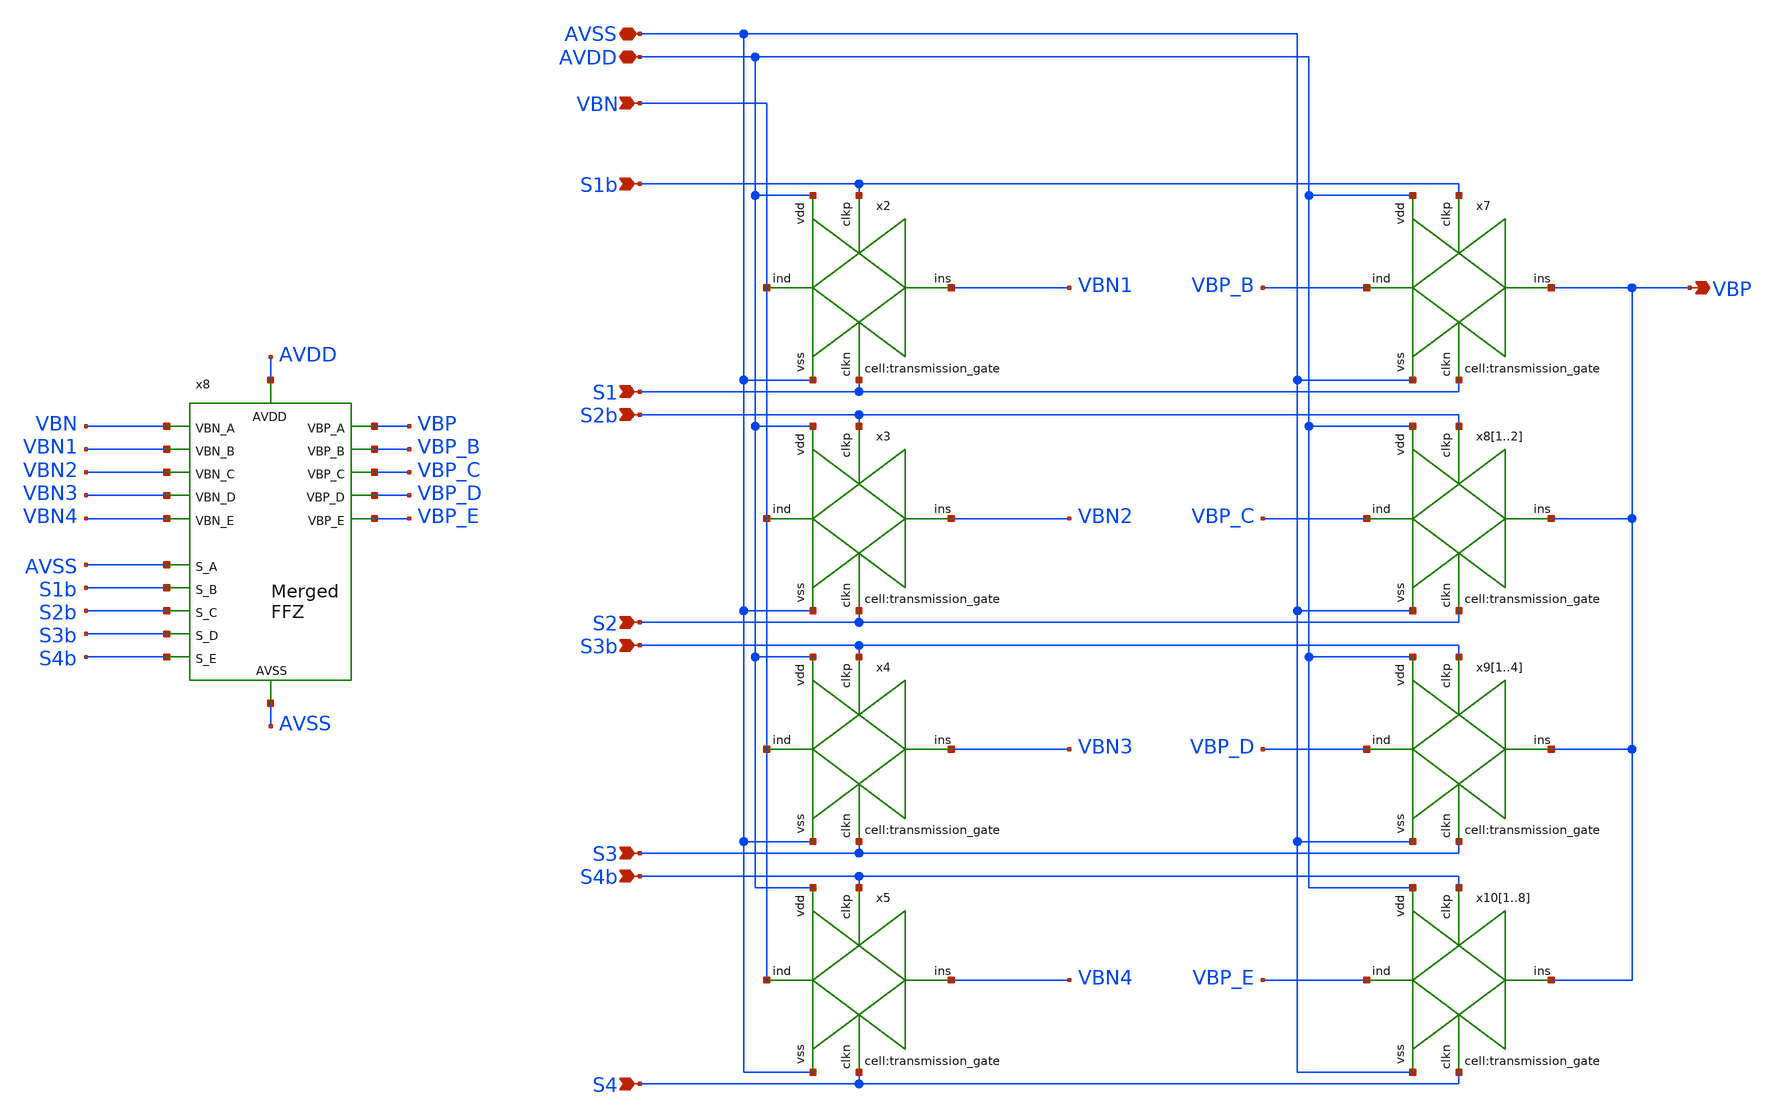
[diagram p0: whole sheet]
** sch_path: designs/libs/core_analog/programmable_ffz/programmable_ffz_v2.sch
**.subckt programmable_ffz_v2 VBN S1b S1 S2b S2 S3b S3 S4b S4 AVSS AVDD VBP
*.ipin VBN
*.ipin S1b
*.ipin S1
*.ipin S2b
*.ipin S2
*.ipin S3b
*.ipin S3
*.ipin S4b
*.ipin S4
*.iopin AVSS
*.iopin AVDD
*.opin VBP
x2 VBN AVSS S1 VBN1 S1b AVDD transmission_gate
x3 VBN AVSS S2 VBN2 S2b AVDD transmission_gate
x4 VBN AVSS S3 VBN3 S3b AVDD transmission_gate
x5 VBN AVSS S4 VBN4 S4b AVDD transmission_gate
x7 VBP_B AVSS S1 VBP S1b AVDD transmission_gate
x81 VBP_C AVSS S2 VBP S2b AVDD transmission_gate
x82 VBP_C AVSS S2 VBP S2b AVDD transmission_gate
x91 VBP_D AVSS S3 VBP S3b AVDD transmission_gate
x92 VBP_D AVSS S3 VBP S3b AVDD transmission_gate
x93 VBP_D AVSS S3 VBP S3b AVDD transmission_gate
x94 VBP_D AVSS S3 VBP S3b AVDD transmission_gate
x101 VBP_E AVSS S4 VBP S4b AVDD transmission_gate
x102 VBP_E AVSS S4 VBP S4b AVDD transmission_gate
x103 VBP_E AVSS S4 VBP S4b AVDD transmission_gate
x104 VBP_E AVSS S4 VBP S4b AVDD transmission_gate
x105 VBP_E AVSS S4 VBP S4b AVDD transmission_gate
x106 VBP_E AVSS S4 VBP S4b AVDD transmission_gate
x107 VBP_E AVSS S4 VBP S4b AVDD transmission_gate
x108 VBP_E AVSS S4 VBP S4b AVDD transmission_gate
x8 VBP_E VBP VBP_C VBN4 VBN VBN2 S4b AVSS S2b AVDD AVSS VBP_B VBP_D VBN1 VBN3 S3b S1b
+ feed_forward_zero_v2_merged
**.ends

* expanding   symbol:  libs/core_analog/transmission_gate/transmission_gate.sym # of pins=6
** sym_path: designs/libs/core_analog/transmission_gate/transmission_gate.sym
** sch_path: designs/libs/core_analog/transmission_gate/transmission_gate.sch
.subckt transmission_gate ind vss clkn ins clkp vdd
*.iopin ind
*.iopin ins
*.iopin clkn
*.iopin clkp
*.iopin vdd
*.iopin vss
XM1 ind clkp ins vdd pfet_03v3 L=0.5u W=3.0u nf=1 ad='int((nf+1)/2) * W/nf * 0.18u' as='int((nf+2)/2) * W/nf * 0.18u'
+ pd='2*int((nf+1)/2) * (W/nf + 0.18u)' ps='2*int((nf+2)/2) * (W/nf + 0.18u)' nrd='0.18u / W' nrs='0.18u / W'
+ sa=0 sb=0 sd=0 m=1
XM2 ind clkn ins vss nfet_03v3 L=0.5u W=1.0u nf=1 ad='int((nf+1)/2) * W/nf * 0.18u' as='int((nf+2)/2) * W/nf * 0.18u'
+ pd='2*int((nf+1)/2) * (W/nf + 0.18u)' ps='2*int((nf+2)/2) * (W/nf + 0.18u)' nrd='0.18u / W' nrs='0.18u / W'
+ sa=0 sb=0 sd=0 m=1
.ends


* expanding   symbol:  libs/core_analog/feed_forward_zero/feed_forward_zero_v2_merged.sym # of
*+ pins=17
** sym_path: designs/libs/core_analog/feed_forward_zero/feed_forward_zero_v2_merged.sym
** sch_path: designs/libs/core_analog/feed_forward_zero/feed_forward_zero_v2_merged.sch
.subckt feed_forward_zero_v2_merged VBP_E VBP_A VBP_C VBN_E VBN_A VBN_C S_E S_A S_C AVDD AVSS VBP_B
+ VBP_D VBN_B VBN_D S_D S_B
*.opin VBP_E
*.iopin AVDD
*.ipin VBN_A
*.opin VBP_A
*.ipin VBN_B
*.ipin S_B
*.opin VBP_B
*.ipin VBN_C
*.ipin S_C
*.opin VBP_C
*.ipin VBN_D
*.ipin S_D
*.opin VBP_D
*.ipin VBN_E
*.ipin S_E
*.ipin S_A
*.iopin AVSS
XM1 VBP_A VBP_A AVDD AVDD pfet_03v3 L=1.5u W=1.1u nf=1 ad='int((nf+1)/2) * W/nf * 0.18u' as='int((nf+2)/2) * W/nf * 0.18u'
+ pd='2*int((nf+1)/2) * (W/nf + 0.18u)' ps='2*int((nf+2)/2) * (W/nf + 0.18u)' nrd='0.18u / W' nrs='0.18u / W'
+ sa=0 sb=0 sd=0 m=1
XM3 VBP_A AVDD net1 AVSS nfet_03v3 L=0.5u W=2.08u nf=1 ad='int((nf+1)/2) * W/nf * 0.18u' as='int((nf+2)/2) * W/nf * 0.18u'
+ pd='2*int((nf+1)/2) * (W/nf + 0.18u)' ps='2*int((nf+2)/2) * (W/nf + 0.18u)' nrd='0.18u / W' nrs='0.18u / W'
+ sa=0 sb=0 sd=0 m=1
XM4 net1 VBN_A AVSS AVSS nfet_03v3 L=0.5u W=2.82u nf=1 ad='int((nf+1)/2) * W/nf * 0.18u' as='int((nf+2)/2) * W/nf * 0.18u'
+ pd='2*int((nf+1)/2) * (W/nf + 0.18u)' ps='2*int((nf+2)/2) * (W/nf + 0.18u)' nrd='0.18u / W' nrs='0.18u / W'
+ sa=0 sb=0 sd=0 m=4
XM7 VBN_A S_A AVSS AVSS nfet_03v3 L=0.5u W=1u nf=1 ad='int((nf+1)/2) * W/nf * 0.18u' as='int((nf+2)/2) * W/nf * 0.18u'
+ pd='2*int((nf+1)/2) * (W/nf + 0.18u)' ps='2*int((nf+2)/2) * (W/nf + 0.18u)' nrd='0.18u / W' nrs='0.18u / W'
+ sa=0 sb=0 sd=0 m=1
XM2 VBP_A VBP_A AVDD AVDD pfet_03v3 L=1.5u W=1.1u nf=1 ad='int((nf+1)/2) * W/nf * 0.18u' as='int((nf+2)/2) * W/nf * 0.18u'
+ pd='2*int((nf+1)/2) * (W/nf + 0.18u)' ps='2*int((nf+2)/2) * (W/nf + 0.18u)' nrd='0.18u / W' nrs='0.18u / W'
+ sa=0 sb=0 sd=0 m=1
XM5 VBP_B VBP_B AVDD AVDD pfet_03v3 L=1.5u W=1.1u nf=1 ad='int((nf+1)/2) * W/nf * 0.18u' as='int((nf+2)/2) * W/nf * 0.18u'
+ pd='2*int((nf+1)/2) * (W/nf + 0.18u)' ps='2*int((nf+2)/2) * (W/nf + 0.18u)' nrd='0.18u / W' nrs='0.18u / W'
+ sa=0 sb=0 sd=0 m=1
XM6 VBP_B AVDD net2 AVSS nfet_03v3 L=0.5u W=2.08u nf=1 ad='int((nf+1)/2) * W/nf * 0.18u' as='int((nf+2)/2) * W/nf * 0.18u'
+ pd='2*int((nf+1)/2) * (W/nf + 0.18u)' ps='2*int((nf+2)/2) * (W/nf + 0.18u)' nrd='0.18u / W' nrs='0.18u / W'
+ sa=0 sb=0 sd=0 m=1
XM8 net2 VBN_B AVSS AVSS nfet_03v3 L=0.5u W=2.82u nf=1 ad='int((nf+1)/2) * W/nf * 0.18u' as='int((nf+2)/2) * W/nf * 0.18u'
+ pd='2*int((nf+1)/2) * (W/nf + 0.18u)' ps='2*int((nf+2)/2) * (W/nf + 0.18u)' nrd='0.18u / W' nrs='0.18u / W'
+ sa=0 sb=0 sd=0 m=4
XM9 VBN_B S_B AVSS AVSS nfet_03v3 L=0.5u W=1u nf=1 ad='int((nf+1)/2) * W/nf * 0.18u' as='int((nf+2)/2) * W/nf * 0.18u'
+ pd='2*int((nf+1)/2) * (W/nf + 0.18u)' ps='2*int((nf+2)/2) * (W/nf + 0.18u)' nrd='0.18u / W' nrs='0.18u / W'
+ sa=0 sb=0 sd=0 m=1
XM10 VBP_B VBP_B AVDD AVDD pfet_03v3 L=1.5u W=1.1u nf=1 ad='int((nf+1)/2) * W/nf * 0.18u' as='int((nf+2)/2) * W/nf * 0.18u'
+ pd='2*int((nf+1)/2) * (W/nf + 0.18u)' ps='2*int((nf+2)/2) * (W/nf + 0.18u)' nrd='0.18u / W' nrs='0.18u / W'
+ sa=0 sb=0 sd=0 m=1
XM11 VBP_C VBP_C AVDD AVDD pfet_03v3 L=1.5u W=1.1u nf=1 ad='int((nf+1)/2) * W/nf * 0.18u' as='int((nf+2)/2) * W/nf * 0.18u'
+ pd='2*int((nf+1)/2) * (W/nf + 0.18u)' ps='2*int((nf+2)/2) * (W/nf + 0.18u)' nrd='0.18u / W' nrs='0.18u / W'
+ sa=0 sb=0 sd=0 m=2
XM12 VBP_C AVDD net3 AVSS nfet_03v3 L=0.5u W=2.08u nf=1 ad='int((nf+1)/2) * W/nf * 0.18u' as='int((nf+2)/2) * W/nf * 0.18u'
+ pd='2*int((nf+1)/2) * (W/nf + 0.18u)' ps='2*int((nf+2)/2) * (W/nf + 0.18u)' nrd='0.18u / W' nrs='0.18u / W'
+ sa=0 sb=0 sd=0 m=2
XM13 net3 VBN_C AVSS AVSS nfet_03v3 L=0.5u W=2.82u nf=1 ad='int((nf+1)/2) * W/nf * 0.18u' as='int((nf+2)/2) * W/nf * 0.18u'
+ pd='2*int((nf+1)/2) * (W/nf + 0.18u)' ps='2*int((nf+2)/2) * (W/nf + 0.18u)' nrd='0.18u / W' nrs='0.18u / W'
+ sa=0 sb=0 sd=0 m=8
XM14 VBN_C S_C AVSS AVSS nfet_03v3 L=0.5u W=1u nf=1 ad='int((nf+1)/2) * W/nf * 0.18u' as='int((nf+2)/2) * W/nf * 0.18u'
+ pd='2*int((nf+1)/2) * (W/nf + 0.18u)' ps='2*int((nf+2)/2) * (W/nf + 0.18u)' nrd='0.18u / W' nrs='0.18u / W'
+ sa=0 sb=0 sd=0 m=2
XM15 VBP_C VBP_C AVDD AVDD pfet_03v3 L=1.5u W=1.1u nf=1 ad='int((nf+1)/2) * W/nf * 0.18u' as='int((nf+2)/2) * W/nf * 0.18u'
+ pd='2*int((nf+1)/2) * (W/nf + 0.18u)' ps='2*int((nf+2)/2) * (W/nf + 0.18u)' nrd='0.18u / W' nrs='0.18u / W'
+ sa=0 sb=0 sd=0 m=2
XM16 VBP_D VBP_D AVDD AVDD pfet_03v3 L=1.5u W=1.1u nf=1 ad='int((nf+1)/2) * W/nf * 0.18u' as='int((nf+2)/2) * W/nf * 0.18u'
+ pd='2*int((nf+1)/2) * (W/nf + 0.18u)' ps='2*int((nf+2)/2) * (W/nf + 0.18u)' nrd='0.18u / W' nrs='0.18u / W'
+ sa=0 sb=0 sd=0 m=4
XM17 VBP_D AVDD net4 AVSS nfet_03v3 L=0.5u W=2.08u nf=1 ad='int((nf+1)/2) * W/nf * 0.18u' as='int((nf+2)/2) * W/nf * 0.18u'
+ pd='2*int((nf+1)/2) * (W/nf + 0.18u)' ps='2*int((nf+2)/2) * (W/nf + 0.18u)' nrd='0.18u / W' nrs='0.18u / W'
+ sa=0 sb=0 sd=0 m=4
XM18 net4 VBN_D AVSS AVSS nfet_03v3 L=0.5u W=2.82u nf=1 ad='int((nf+1)/2) * W/nf * 0.18u' as='int((nf+2)/2) * W/nf * 0.18u'
+ pd='2*int((nf+1)/2) * (W/nf + 0.18u)' ps='2*int((nf+2)/2) * (W/nf + 0.18u)' nrd='0.18u / W' nrs='0.18u / W'
+ sa=0 sb=0 sd=0 m=16
XM19 VBN_D S_D AVSS AVSS nfet_03v3 L=0.5u W=1u nf=1 ad='int((nf+1)/2) * W/nf * 0.18u' as='int((nf+2)/2) * W/nf * 0.18u'
+ pd='2*int((nf+1)/2) * (W/nf + 0.18u)' ps='2*int((nf+2)/2) * (W/nf + 0.18u)' nrd='0.18u / W' nrs='0.18u / W'
+ sa=0 sb=0 sd=0 m=4
XM20 VBP_D VBP_D AVDD AVDD pfet_03v3 L=1.5u W=1.1u nf=1 ad='int((nf+1)/2) * W/nf * 0.18u' as='int((nf+2)/2) * W/nf * 0.18u'
+ pd='2*int((nf+1)/2) * (W/nf + 0.18u)' ps='2*int((nf+2)/2) * (W/nf + 0.18u)' nrd='0.18u / W' nrs='0.18u / W'
+ sa=0 sb=0 sd=0 m=4
XM21 VBP_E VBP_E AVDD AVDD pfet_03v3 L=1.5u W=1.1u nf=1 ad='int((nf+1)/2) * W/nf * 0.18u' as='int((nf+2)/2) * W/nf * 0.18u'
+ pd='2*int((nf+1)/2) * (W/nf + 0.18u)' ps='2*int((nf+2)/2) * (W/nf + 0.18u)' nrd='0.18u / W' nrs='0.18u / W'
+ sa=0 sb=0 sd=0 m=8
XM22 VBP_E AVDD net5 AVSS nfet_03v3 L=0.5u W=2.08u nf=1 ad='int((nf+1)/2) * W/nf * 0.18u' as='int((nf+2)/2) * W/nf * 0.18u'
+ pd='2*int((nf+1)/2) * (W/nf + 0.18u)' ps='2*int((nf+2)/2) * (W/nf + 0.18u)' nrd='0.18u / W' nrs='0.18u / W'
+ sa=0 sb=0 sd=0 m=8
XM23 net5 VBN_E AVSS AVSS nfet_03v3 L=0.5u W=2.82u nf=1 ad='int((nf+1)/2) * W/nf * 0.18u' as='int((nf+2)/2) * W/nf * 0.18u'
+ pd='2*int((nf+1)/2) * (W/nf + 0.18u)' ps='2*int((nf+2)/2) * (W/nf + 0.18u)' nrd='0.18u / W' nrs='0.18u / W'
+ sa=0 sb=0 sd=0 m=32
XM24 VBN_E S_E AVSS AVSS nfet_03v3 L=0.5u W=1u nf=1 ad='int((nf+1)/2) * W/nf * 0.18u' as='int((nf+2)/2) * W/nf * 0.18u'
+ pd='2*int((nf+1)/2) * (W/nf + 0.18u)' ps='2*int((nf+2)/2) * (W/nf + 0.18u)' nrd='0.18u / W' nrs='0.18u / W'
+ sa=0 sb=0 sd=0 m=8
XM25 VBP_E VBP_E AVDD AVDD pfet_03v3 L=1.5u W=1.1u nf=1 ad='int((nf+1)/2) * W/nf * 0.18u' as='int((nf+2)/2) * W/nf * 0.18u'
+ pd='2*int((nf+1)/2) * (W/nf + 0.18u)' ps='2*int((nf+2)/2) * (W/nf + 0.18u)' nrd='0.18u / W' nrs='0.18u / W'
+ sa=0 sb=0 sd=0 m=8
.ends

.end
